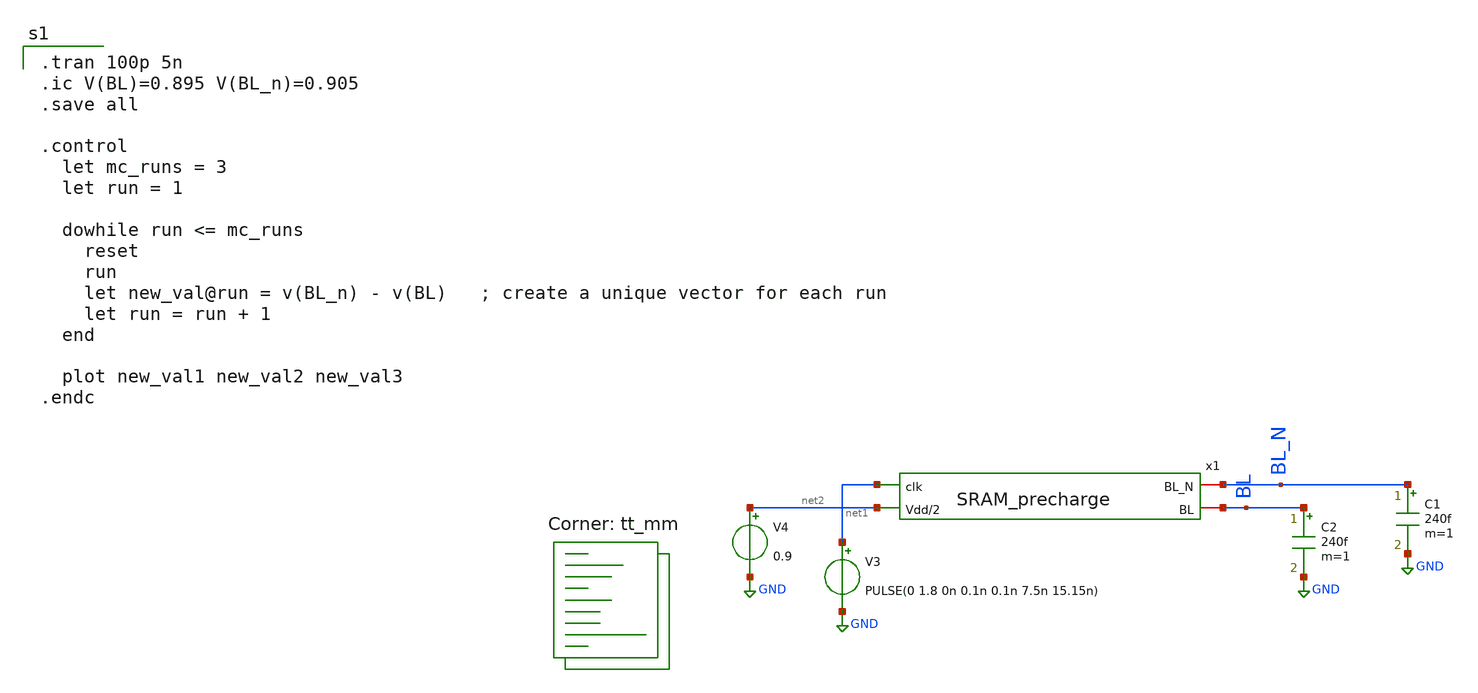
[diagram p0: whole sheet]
** sch_path: analog/schematics/tb.sch
**.subckt tb
x1 BL_N BL net1 net2 SRAM_precharge
C1 BL_N GND 240f m=1
C2 BL GND 240f m=1
V3 net1 GND PULSE(0 1.8 0n 0.1n 0.1n 7.5n 15.15n)
V4 net2 GND 0.9
**** begin user architecture code

.tran 100p 5n
.ic V(BL)=0.895 V(BL_n)=0.905
.save all

.control
  let mc_runs = 3
  let run = 1

  dowhile run <= mc_runs
    reset
    run
    let new_val@run = v(BL_n) - v(BL)   ; create a unique vector for each run
    let run = run + 1
  end

  plot new_val1 new_val2 new_val3
.endc

.lib $::SKYWATER_MODELS/sky130.lib.spice tt_mm
**** end user architecture code
**.ends
.GLOBAL GND
.end
